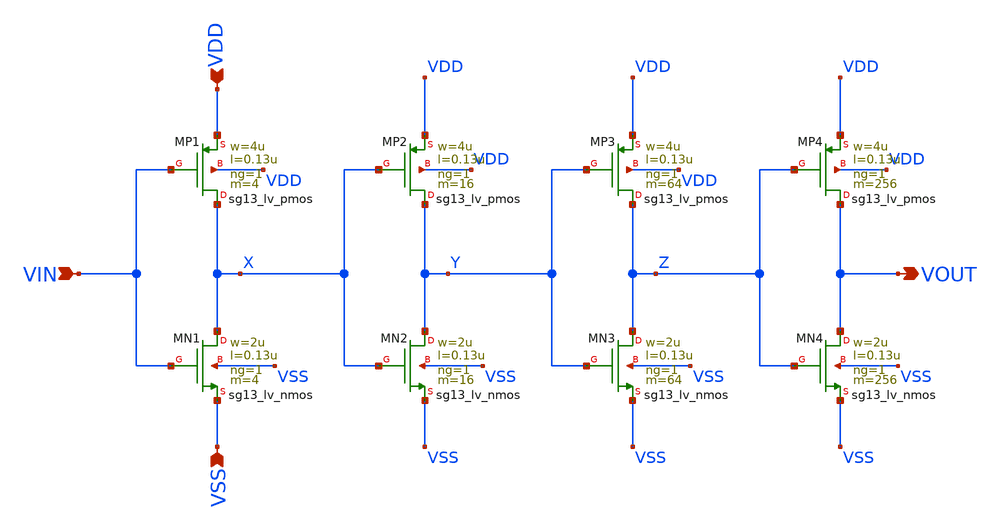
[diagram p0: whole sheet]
** sch_path: work/gate_buff_pad/xschem/gate_buff_pad.sch
**.subckt gate_buff_pad VDD VIN VSS VOUT
*.ipin VDD
*.ipin VIN
*.ipin VSS
*.opin VOUT
XMN1 X VIN VSS VSS sg13_lv_nmos w=2u l=0.13u ng=1 m=4 mm_ok=1
XMP1 X VIN VDD VDD sg13_lv_pmos w=4u l=0.13u ng=1 m=4 mm_ok=1
XMN2 Y X VSS VSS sg13_lv_nmos w=2u l=0.13u ng=1 m=16 mm_ok=1
XMP2 Y X VDD VDD sg13_lv_pmos w=4u l=0.13u ng=1 m=16 mm_ok=1
XMN3 Z Y VSS VSS sg13_lv_nmos w=2u l=0.13u ng=1 m=64 mm_ok=1
XMP3 Z Y VDD VDD sg13_lv_pmos w=4u l=0.13u ng=1 m=64 mm_ok=1
XMN4 VOUT Z VSS VSS sg13_lv_nmos w=2u l=0.13u ng=1 m=256 mm_ok=1
XMP4 VOUT Z VDD VDD sg13_lv_pmos w=4u l=0.13u ng=1 m=256 mm_ok=1
**.ends
.end
